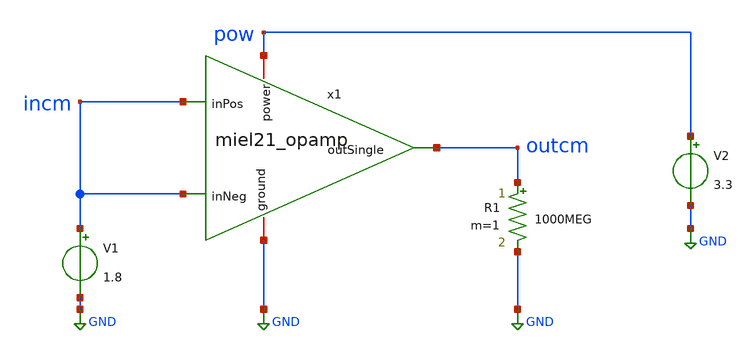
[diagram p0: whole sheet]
** sch_path: dev/opamp/miel21_tb_opamp_op.sch
**.subckt miel21_tb_opamp_op
x1 pow outcm incm incm GND miel21_opamp
V1 incm GND 1.8
V2 pow GND 3.3
R1 outcm GND 1000MEG m=1
**** begin user architecture code


.lib "/usr/share/pdk/sky130A/libs.tech/ngspice/sky130.lib.spice" tt
.param mc_mm_switch=0
.param mc_pr_switch=0
.save incm outcm pow x1.nsources x1.d1 x1.d2 x1.bias
.save @m.x1.xm1.msky130_fd_pr__nfet_g5v0d10v5[id]
.save @m.x1.xm2.msky130_fd_pr__nfet_g5v0d10v5[id]
.save @m.x1.xm3.msky130_fd_pr__nfet_g5v0d10v5[id]
.save @m.x1.xm4.msky130_fd_pr__nfet_g5v0d10v5[id]
.save @m.x1.xm5.msky130_fd_pr__nfet_g5v0d10v5[id]
.save @m.x1.xm6.msky130_fd_pr__pfet_g5v0d10v5[id]
.save @m.x1.xm7.msky130_fd_pr__pfet_g5v0d10v5[id]
.save @m.x1.xm8.msky130_fd_pr__pfet_g5v0d10v5[id] @m.x1.xm1.msky130_fd_pr__nfet_g5v0d10v5[gm] @m.x1.xm2.msky130_fd_pr__nfet_g5v0d10v5[gm] @m.x1.xm3.msky130_fd_pr__nfet_g5v0d10v5[gm] @m.x1.xm4.msky130_fd_pr__nfet_g5v0d10v5[gm] @m.x1.xm5.msky130_fd_pr__nfet_g5v0d10v5[gm] @m.x1.xm6.msky130_fd_pr__pfet_g5v0d10v5[gm] @m.x1.xm7.msky130_fd_pr__pfet_g5v0d10v5[gm] @m.x1.xm8.msky130_fd_pr__pfet_g5v0d10v5[gm] @m.x1.xm1.msky130_fd_pr__nfet_g5v0d10v5[vdsat] @m.x1.xm2.msky130_fd_pr__nfet_g5v0d10v5[vdsat] @m.x1.xm3.msky130_fd_pr__nfet_g5v0d10v5[vdsat] @m.x1.xm4.msky130_fd_pr__nfet_g5v0d10v5[vdsat] @m.x1.xm5.msky130_fd_pr__nfet_g5v0d10v5[vdsat] @m.x1.xm6.msky130_fd_pr__pfet_g5v0d10v5[vdsat] @m.x1.xm7.msky130_fd_pr__pfet_g5v0d10v5[vdsat] @m.x1.xm8.msky130_fd_pr__pfet_g5v0d10v5[vdsat] @m.x1.xm1.msky130_fd_pr__nfet_g5v0d10v5[vds] @m.x1.xm2.msky130_fd_pr__nfet_g5v0d10v5[vds] @m.x1.xm3.msky130_fd_pr__nfet_g5v0d10v5[vds] @m.x1.xm4.msky130_fd_pr__nfet_g5v0d10v5[vds] @m.x1.xm5.msky130_fd_pr__nfet_g5v0d10v5[vds] @m.x1.xm6.msky130_fd_pr__pfet_g5v0d10v5[vds] @m.x1.xm7.msky130_fd_pr__pfet_g5v0d10v5[vds] @m.x1.xm8.msky130_fd_pr__pfet_g5v0d10v5[vds] @m.x1.xm1.msky130_fd_pr__nfet_g5v0d10v5[vgs] @m.x1.xm2.msky130_fd_pr__nfet_g5v0d10v5[vgs] @m.x1.xm3.msky130_fd_pr__nfet_g5v0d10v5[vgs] @m.x1.xm4.msky130_fd_pr__nfet_g5v0d10v5[vgs] @m.x1.xm5.msky130_fd_pr__nfet_g5v0d10v5[vgs] @m.x1.xm6.msky130_fd_pr__pfet_g5v0d10v5[vgs] @m.x1.xm7.msky130_fd_pr__pfet_g5v0d10v5[vgs] @m.x1.xm8.msky130_fd_pr__pfet_g5v0d10v5[vgs] @m.x1.xm1.msky130_fd_pr__nfet_g5v0d10v5[vth] @m.x1.xm2.msky130_fd_pr__nfet_g5v0d10v5[vth] @m.x1.xm3.msky130_fd_pr__nfet_g5v0d10v5[vth] @m.x1.xm4.msky130_fd_pr__nfet_g5v0d10v5[vth] @m.x1.xm5.msky130_fd_pr__nfet_g5v0d10v5[vth] @m.x1.xm6.msky130_fd_pr__pfet_g5v0d10v5[vth] @m.x1.xm7.msky130_fd_pr__pfet_g5v0d10v5[vth] @m.x1.xm8.msky130_fd_pr__pfet_g5v0d10v5[vth]
.op

.control
set wr_vecnames
set wr_singlescale

run

wrdata miel21_tb_opamp_op.res incm outcm pow x1.nsources x1.d1 x1.d2 x1.bias
+ @m.x1.xm1.msky130_fd_pr__nfet_g5v0d10v5[id] @m.x1.xm2.msky130_fd_pr__nfet_g5v0d10v5[id] @m.x1.xm3.msky130_fd_pr__nfet_g5v0d10v5[id]
+ @m.x1.xm4.msky130_fd_pr__nfet_g5v0d10v5[id] @m.x1.xm5.msky130_fd_pr__nfet_g5v0d10v5[id] @m.x1.xm6.msky130_fd_pr__pfet_g5v0d10v5[id]
+ @m.x1.xm7.msky130_fd_pr__pfet_g5v0d10v5[id] @m.x1.xm8.msky130_fd_pr__pfet_g5v0d10v5[id] @m.x1.xm1.msky130_fd_pr__nfet_g5v0d10v5[gm]
+ @m.x1.xm2.msky130_fd_pr__nfet_g5v0d10v5[gm] @m.x1.xm3.msky130_fd_pr__nfet_g5v0d10v5[gm] @m.x1.xm4.msky130_fd_pr__nfet_g5v0d10v5[gm]
+ @m.x1.xm5.msky130_fd_pr__nfet_g5v0d10v5[gm] @m.x1.xm6.msky130_fd_pr__pfet_g5v0d10v5[gm] @m.x1.xm7.msky130_fd_pr__pfet_g5v0d10v5[gm]
+ @m.x1.xm8.msky130_fd_pr__pfet_g5v0d10v5[gm] @m.x1.xm1.msky130_fd_pr__nfet_g5v0d10v5[vdsat] @m.x1.xm2.msky130_fd_pr__nfet_g5v0d10v5[vdsat]
+ @m.x1.xm3.msky130_fd_pr__nfet_g5v0d10v5[vdsat] @m.x1.xm4.msky130_fd_pr__nfet_g5v0d10v5[vdsat] @m.x1.xm5.msky130_fd_pr__nfet_g5v0d10v5[vdsat]
+ @m.x1.xm6.msky130_fd_pr__pfet_g5v0d10v5[vdsat] @m.x1.xm7.msky130_fd_pr__pfet_g5v0d10v5[vdsat] @m.x1.xm8.msky130_fd_pr__pfet_g5v0d10v5[vdsat]
+ @m.x1.xm1.msky130_fd_pr__nfet_g5v0d10v5[vds] @m.x1.xm2.msky130_fd_pr__nfet_g5v0d10v5[vds] @m.x1.xm3.msky130_fd_pr__nfet_g5v0d10v5[vds]
+ @m.x1.xm4.msky130_fd_pr__nfet_g5v0d10v5[vds] @m.x1.xm5.msky130_fd_pr__nfet_g5v0d10v5[vds] @m.x1.xm6.msky130_fd_pr__pfet_g5v0d10v5[vds]
+ @m.x1.xm7.msky130_fd_pr__pfet_g5v0d10v5[vds] @m.x1.xm8.msky130_fd_pr__pfet_g5v0d10v5[vds] @m.x1.xm1.msky130_fd_pr__nfet_g5v0d10v5[vgs]
+ @m.x1.xm2.msky130_fd_pr__nfet_g5v0d10v5[vgs] @m.x1.xm3.msky130_fd_pr__nfet_g5v0d10v5[vgs] @m.x1.xm4.msky130_fd_pr__nfet_g5v0d10v5[vgs]
+ @m.x1.xm5.msky130_fd_pr__nfet_g5v0d10v5[vgs] @m.x1.xm6.msky130_fd_pr__pfet_g5v0d10v5[vgs] @m.x1.xm7.msky130_fd_pr__pfet_g5v0d10v5[vgs]
+ @m.x1.xm8.msky130_fd_pr__pfet_g5v0d10v5[vgs] @m.x1.xm1.msky130_fd_pr__nfet_g5v0d10v5[vth] @m.x1.xm2.msky130_fd_pr__nfet_g5v0d10v5[vth]
+ @m.x1.xm3.msky130_fd_pr__nfet_g5v0d10v5[vth] @m.x1.xm4.msky130_fd_pr__nfet_g5v0d10v5[vth] @m.x1.xm5.msky130_fd_pr__nfet_g5v0d10v5[vth]
+ @m.x1.xm6.msky130_fd_pr__pfet_g5v0d10v5[vth] @m.x1.xm7.msky130_fd_pr__pfet_g5v0d10v5[vth] @m.x1.xm8.msky130_fd_pr__pfet_g5v0d10v5[vth]
.endc


**** end user architecture code
**.ends

* expanding   symbol:  miel21_opamp.sym # of pins=5
** sym_path: dev/opamp/miel21_opamp.sym
** sch_path: dev/opamp/miel21_opamp.sch
.subckt miel21_opamp power outSingle inPos inNeg ground
*.ipin inPos
*.ipin inNeg
*.opin outSingle
*.iopin power
*.iopin ground
XM6 d1 d1 power power sky130_fd_pr__pfet_g5v0d10v5 L=0.5 W=21 nf=3 ad='int((nf+1)/2) * W/nf * 0.29' as='int((nf+2)/2) * W/nf * 0.29'
+ pd='2*int((nf+1)/2) * (W/nf + 0.29)' ps='2*int((nf+2)/2) * (W/nf + 0.29)' nrd='0.29 / W' nrs='0.29 / W'
+ sa=0 sb=0 sd=0 mult=1 m=1
XM7 d2 d1 power power sky130_fd_pr__pfet_g5v0d10v5 L=0.5 W=21 nf=3 ad='int((nf+1)/2) * W/nf * 0.29' as='int((nf+2)/2) * W/nf * 0.29'
+ pd='2*int((nf+1)/2) * (W/nf + 0.29)' ps='2*int((nf+2)/2) * (W/nf + 0.29)' nrd='0.29 / W' nrs='0.29 / W'
+ sa=0 sb=0 sd=0 mult=1 m=1
XM8 outSingle d2 power power sky130_fd_pr__pfet_g5v0d10v5 L=0.5 W=260 nf=20 ad='int((nf+1)/2) * W/nf * 0.29'
+ as='int((nf+2)/2) * W/nf * 0.29' pd='2*int((nf+1)/2) * (W/nf + 0.29)' ps='2*int((nf+2)/2) * (W/nf + 0.29)'
+ nrd='0.29 / W' nrs='0.29 / W' sa=0 sb=0 sd=0 mult=1 m=1
XM1 d1 inPos nsources ground sky130_fd_pr__nfet_g5v0d10v5 L=0.5 W=5 nf=1 ad='int((nf+1)/2) * W/nf * 0.29'
+ as='int((nf+2)/2) * W/nf * 0.29' pd='2*int((nf+1)/2) * (W/nf + 0.29)' ps='2*int((nf+2)/2) * (W/nf + 0.29)'
+ nrd='0.29 / W' nrs='0.29 / W' sa=0 sb=0 sd=0 mult=1 m=1
XM2 d2 inNeg nsources ground sky130_fd_pr__nfet_g5v0d10v5 L=0.5 W=5 nf=1 ad='int((nf+1)/2) * W/nf * 0.29'
+ as='int((nf+2)/2) * W/nf * 0.29' pd='2*int((nf+1)/2) * (W/nf + 0.29)' ps='2*int((nf+2)/2) * (W/nf + 0.29)'
+ nrd='0.29 / W' nrs='0.29 / W' sa=0 sb=0 sd=0 mult=1 m=1
XM3 bias bias ground ground sky130_fd_pr__nfet_g5v0d10v5 L=0.5 W=10 nf=2 ad='int((nf+1)/2) * W/nf * 0.29'
+ as='int((nf+2)/2) * W/nf * 0.29' pd='2*int((nf+1)/2) * (W/nf + 0.29)' ps='2*int((nf+2)/2) * (W/nf + 0.29)'
+ nrd='0.29 / W' nrs='0.29 / W' sa=0 sb=0 sd=0 mult=1 m=1
XM4 nsources bias ground ground sky130_fd_pr__nfet_g5v0d10v5 L=0.5 W=10 nf=2 ad='int((nf+1)/2) * W/nf * 0.29'
+ as='int((nf+2)/2) * W/nf * 0.29' pd='2*int((nf+1)/2) * (W/nf + 0.29)' ps='2*int((nf+2)/2) * (W/nf + 0.29)'
+ nrd='0.29 / W' nrs='0.29 / W' sa=0 sb=0 sd=0 mult=1 m=1
XM5 outSingle bias ground ground sky130_fd_pr__nfet_g5v0d10v5 L=0.5 W=48 nf=8 ad='int((nf+1)/2) * W/nf * 0.29'
+ as='int((nf+2)/2) * W/nf * 0.29' pd='2*int((nf+1)/2) * (W/nf + 0.29)' ps='2*int((nf+2)/2) * (W/nf + 0.29)'
+ nrd='0.29 / W' nrs='0.29 / W' sa=0 sb=0 sd=0 mult=1 m=1
XR1 bias net2 ground sky130_fd_pr__res_xhigh_po_0p69 L=6 mult=1 m=1
XC1 outSingle d2 sky130_fd_pr__cap_mim_m3_1 W=10 L=14 MF=1 m=1
XR2 net2 net1 ground sky130_fd_pr__res_xhigh_po_0p69 L=6 mult=1 m=1
XR3 net1 power ground sky130_fd_pr__res_xhigh_po_0p69 L=6 mult=1 m=1
.ends

.GLOBAL GND
.end
